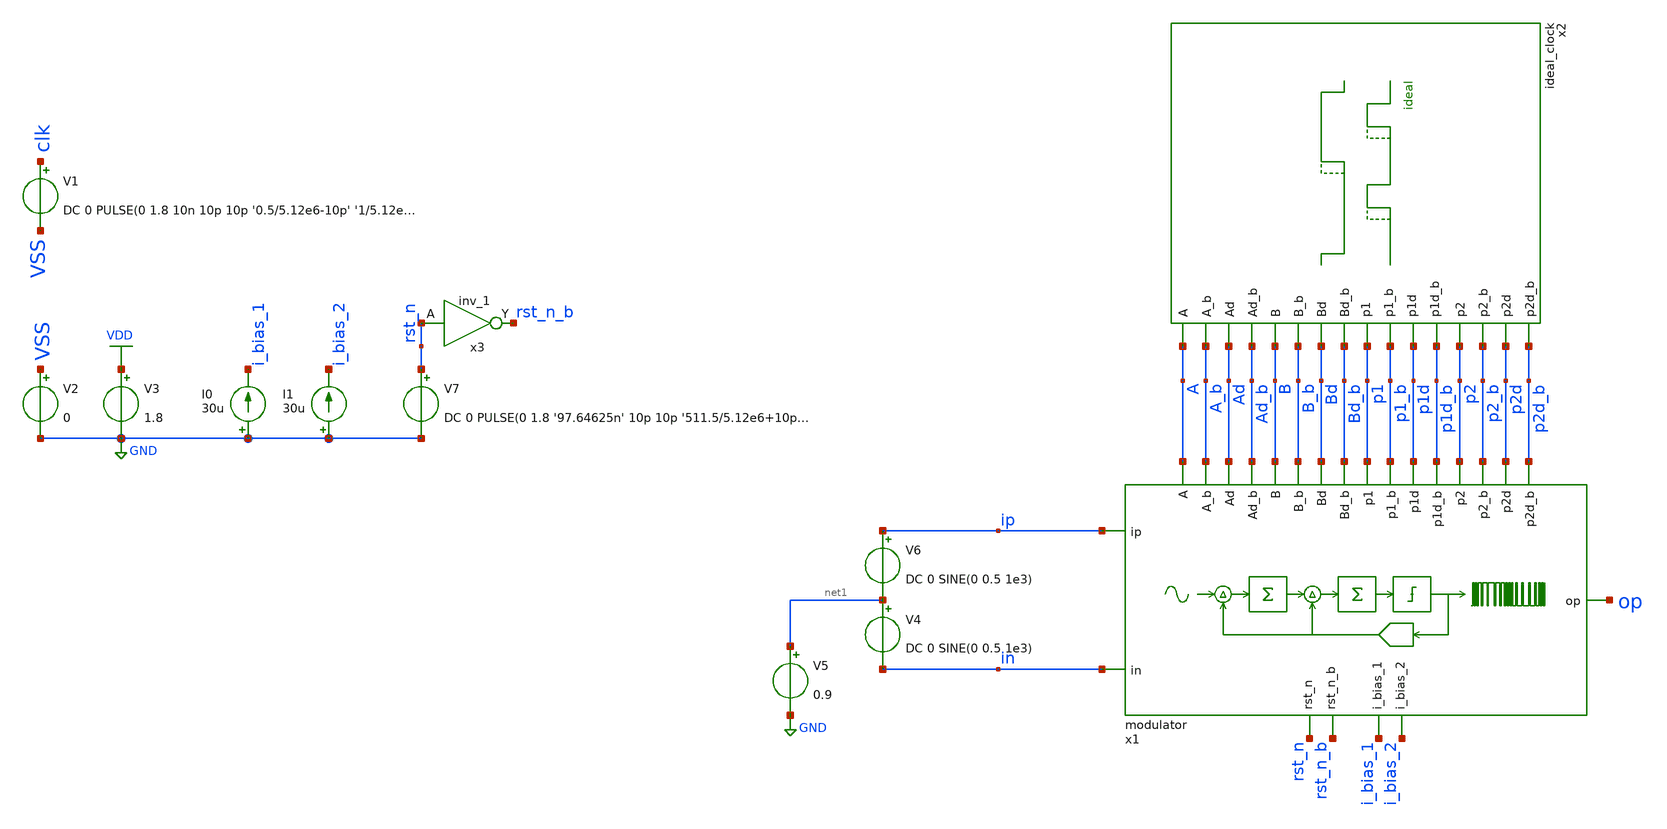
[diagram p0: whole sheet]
** sch_path: verification/analog_modulator/modulator_tb_ideal_clock.sch
**.subckt modulator_tb_ideal_clock
V1 clk VSS DC 0 PULSE(0 1.8 10n 10p 10p '0.5/5.12e6-10p' '1/5.12e6')
V2 VSS GND 0
V3 VDD GND 1.8
I0 GND i_bias_1 30u
I1 GND i_bias_2 30u
V5 net1 GND 0.9
V6 ip net1 DC 0 SINE(0 0.5 1e3)
V4 net1 in DC 0 SINE(0 0.5 1e3)
x1 ip in A B A_b B_b Ad Bd Ad_b Bd_b p1 p1_b p2 p2_b p1d p1d_b p2d p2d_b i_bias_1 i_bias_2 rst_n
+ rst_n_b op VDD VSS modulator
x3 rst_n GND GND VDD VDD rst_n_b sky130_fd_sc_hd__inv_1
V7 rst_n GND DC 0 PULSE(0 1.8 '97.64625n' 10p 10p '511.5/5.12e6+10p' '512/5.12e6')
x2 A A_b Ad Ad_b Bd_b Bd B_b B p2 p2_b p2d p2d_b p1d_b p1d p1_b p1 97.64625n VDD VSS ideal_clock
**** begin user architecture code

** opencircuitdesign pdks install
.lib /farmshare/home/classes/ee/372/PDKs/open_pdks_1.0.310/sky130/sky130A/libs.tech/ngspice/sky130.lib.spice tt
.inc /farmshare/home/classes/ee/372/PDKs/open_pdks_1.0.310/sky130/sky130A/libs.ref/sky130_fd_sc_hd/spice/sky130_fd_sc_hd.spice



.control
tran 1u 50u
*let i_diff = v(ip) - v(in)
*let vc1 = v(c1l) - v(c1r)
*let i1_diff = v(ip1) - v(in1)
*let o1_diff = v(op1) - v(on1)
*let vc3 = v(c3l) - v(c3r)
*let vc4 = v(c4l) - v(c3r)
*let i2_diff = v(ip2) - v(in2)
*let o2_diff = v(op2) - v(on2)
save all
write modulator_tb_ideal_clock_mavg2.raw
.endc


**** end user architecture code
**.ends
.GLOBAL GND
.GLOBAL VDD
.end
